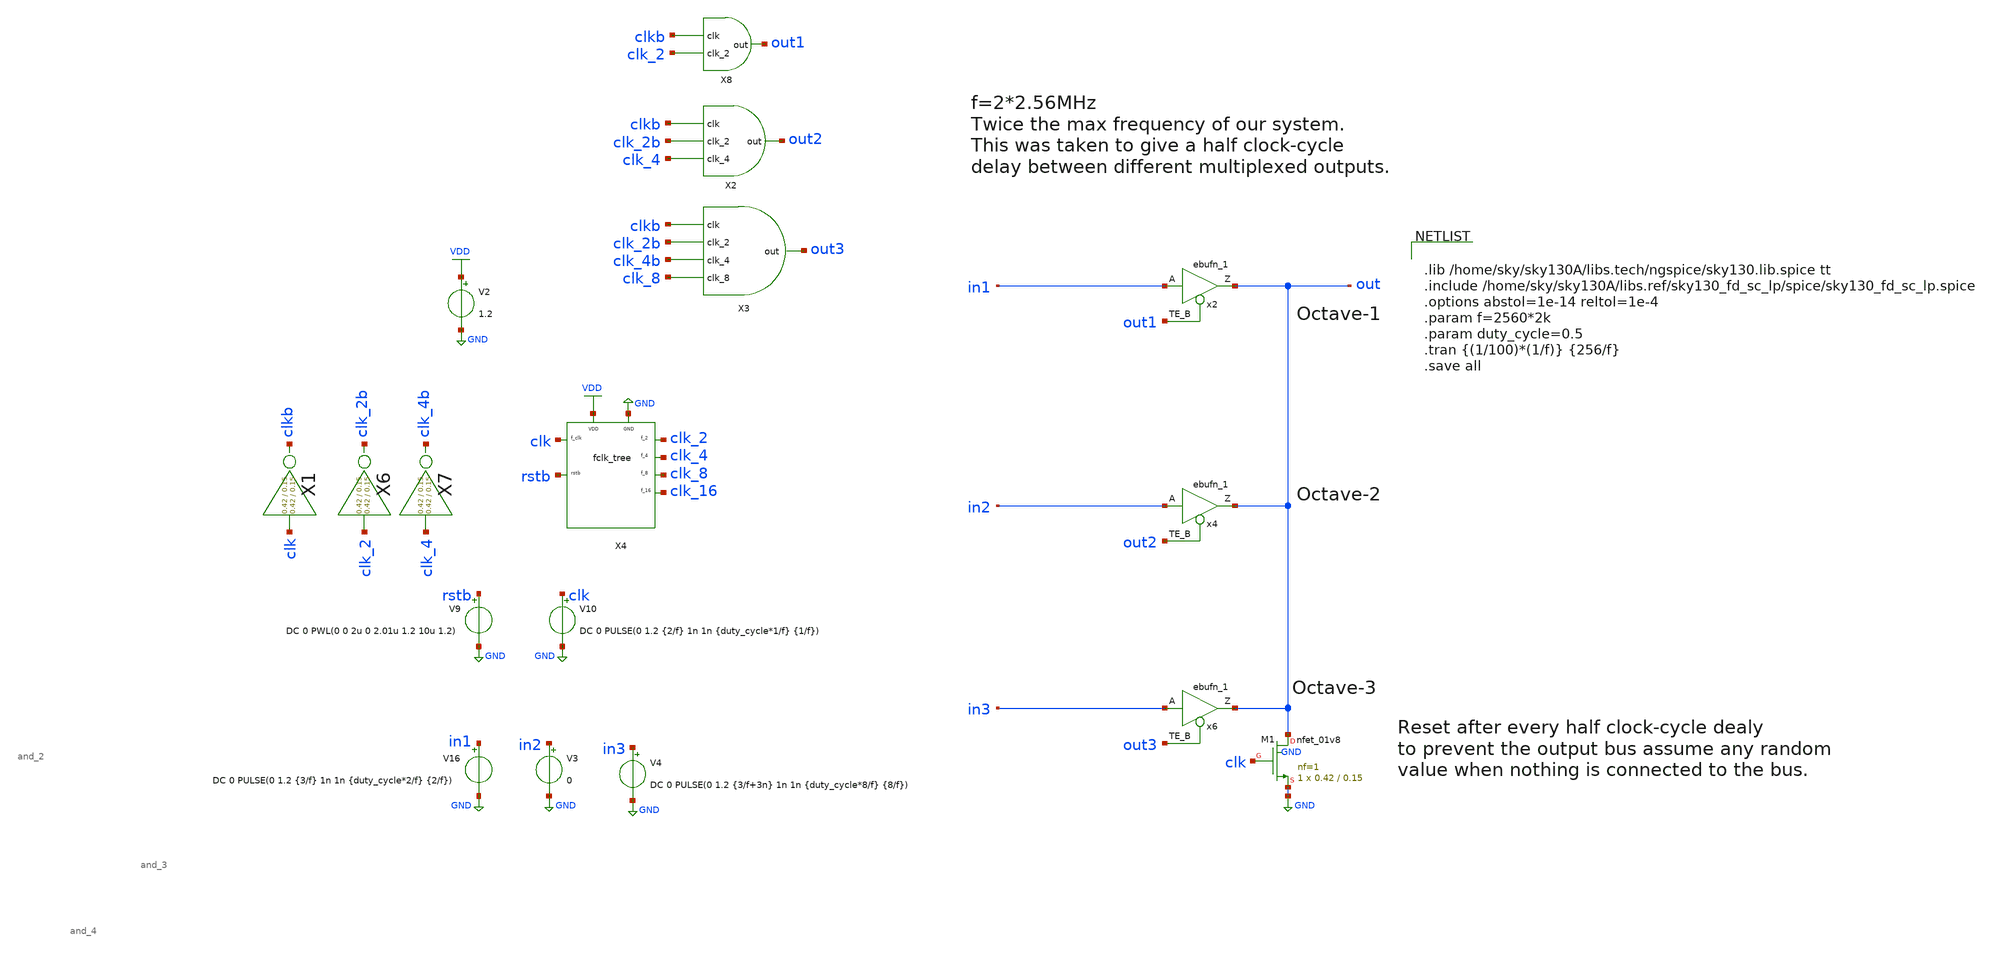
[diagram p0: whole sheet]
** sch_path: xschem/readout/sample_ro_2.sch
**.subckt sample_ro_2
V2 VDD GND 1.2
X4 clk rstb clk_2 clk_4 VDD GND clk_8 clk_16 fclk_tree
V10 clk GND DC 0 PULSE(0 1.2 {2/f} 1n 1n {duty_cycle*1/f} {1/f})
x4 in2 out2 GND GND VDD VDD out sky130_fd_sc_lp__ebufn_1
x6 in3 out3 GND GND VDD VDD out sky130_fd_sc_lp__ebufn_1
V9 rstb GND DC 0 PWL(0 0 2u 0 2.01u 1.2 10u 1.2)
x2 in1 out1 GND GND VDD VDD out sky130_fd_sc_lp__ebufn_1
XM1 out clk GND GND sky130_fd_pr__nfet_01v8 L=0.15 W=0.42 nf=1 ad='int((nf+1)/2) * W/nf * 0.29' as='int((nf+2)/2) * W/nf * 0.29'
+ pd='2*int((nf+1)/2) * (W/nf + 0.29)' ps='2*int((nf+2)/2) * (W/nf + 0.29)' nrd='0.29 / W' nrs='0.29 / W'
+ sa=0 sb=0 sd=0 mult=1 m=1
X1 clk clkb inv Wpmos=0.42 Lpmos=0.15 Wnmos=0.42 Lnmos=0.15
V16 in1 GND DC 0 PULSE(0 1.2 {3/f} 1n 1n {duty_cycle*2/f} {2/f})
V3 in2 GND 0
V4 in3 GND DC 0 PULSE(0 1.2 {3/f+3n} 1n 1n {duty_cycle*8/f} {8/f})
X6 clk_2 clk_2b inv Wpmos=0.42 Lpmos=0.15 Wnmos=0.42 Lnmos=0.15
X7 clk_4 clk_4b inv Wpmos=0.42 Lpmos=0.15 Wnmos=0.42 Lnmos=0.15
X8 clkb clk_2 out1 and_2
X2 clkb clk_2b clk_4 out2 and_3
X3 clkb clk_2b clk_4b clk_8 out3 and_4
**** begin user architecture code


.lib /home/sky/sky130A/libs.tech/ngspice/sky130.lib.spice tt
.include /home/sky/sky130A/libs.ref/sky130_fd_sc_lp/spice/sky130_fd_sc_lp.spice
.options abstol=1e-14 reltol=1e-4
.param f=2560*2k
.param duty_cycle=0.5
.tran {(1/100)*(1/f)} {256/f}
.save all


**** end user architecture code
**.ends

* expanding   symbol:  readout/fclk_tree.sym # of pins=8
** sym_path: xschem/readout/fclk_tree.sym
** sch_path: xschem/readout/fclk_tree.sch
.subckt fclk_tree f_clk rstb f_2 f_4 VDD GND f_8 f_16
*.iopin VDD
*.iopin GND
*.ipin rstb
*.opin f_2
*.opin f_4
*.opin f_8
*.opin f_16
*.ipin f_clk
x2 f_clk net1 rstb gnd gnd vdd vdd f_2 net1 sky130_fd_sc_lp__dfrbp_1
x4 f_2 net2 rstb gnd gnd vdd vdd f_4 net2 sky130_fd_sc_lp__dfrbp_1
x1 f_4 net3 rstb gnd gnd vdd vdd f_8 net3 sky130_fd_sc_lp__dfrbp_1
x6 f_8 net4 rstb gnd gnd vdd vdd f_16 net4 sky130_fd_sc_lp__dfrbp_1
.ends


* expanding   symbol:  inv/inv.sym # of pins=2
** sym_path: xschem/inv/inv.sym
** sch_path: xschem/inv/inv.sch
.subckt inv in out  Wpmos=3 Lpmos=0.18 Wnmos=1 Lnmos=0.18
*.ipin in
*.iopin out
XM1 out in GND GND sky130_fd_pr__nfet_01v8 L=Lnmos W=Wnmos nf=1 ad='int((nf+1)/2) * W/nf * 0.29' as='int((nf+2)/2) * W/nf * 0.29'
+ pd='2*int((nf+1)/2) * (W/nf + 0.29)' ps='2*int((nf+2)/2) * (W/nf + 0.29)' nrd='0.29 / W' nrs='0.29 / W'
+ sa=0 sb=0 sd=0 mult=1 m=1
XM2 out in VDD VDD sky130_fd_pr__pfet_01v8 L=Lpmos W=Wpmos nf=1 ad='int((nf+1)/2) * W/nf * 0.29' as='int((nf+2)/2) * W/nf * 0.29'
+ pd='2*int((nf+1)/2) * (W/nf + 0.29)' ps='2*int((nf+2)/2) * (W/nf + 0.29)' nrd='0.29 / W' nrs='0.29 / W'
+ sa=0 sb=0 sd=0 mult=1 m=1
.ends


* expanding   symbol:  and_set/and_2.sym # of pins=3
** sym_path: xschem/and_set/and_2.sym
** sch_path: xschem/and_set/and_2.sch
.subckt and_2 clk clk_2 out
*.ipin clk
*.ipin clk_2
*.opin out
XM1 out clk_2 VDD VDD sky130_fd_pr__pfet_01v8 L=0.15 W=0.42 nf=1 ad='int((nf+1)/2) * W/nf * 0.29' as='int((nf+2)/2) * W/nf * 0.29'
+ pd='2*int((nf+1)/2) * (W/nf + 0.29)' ps='2*int((nf+2)/2) * (W/nf + 0.29)' nrd='0.29 / W' nrs='0.29 / W'
+ sa=0 sb=0 sd=0 mult=1 m=1
XM2 out clk net1 GND sky130_fd_pr__nfet_01v8 L=0.15 W=0.42 nf=1 ad='int((nf+1)/2) * W/nf * 0.29' as='int((nf+2)/2) * W/nf * 0.29'
+ pd='2*int((nf+1)/2) * (W/nf + 0.29)' ps='2*int((nf+2)/2) * (W/nf + 0.29)' nrd='0.29 / W' nrs='0.29 / W'
+ sa=0 sb=0 sd=0 mult=1 m=1
XM3 net1 clk_2 GND GND sky130_fd_pr__nfet_01v8 L=0.15 W=0.42 nf=1 ad='int((nf+1)/2) * W/nf * 0.29' as='int((nf+2)/2) * W/nf * 0.29'
+ pd='2*int((nf+1)/2) * (W/nf + 0.29)' ps='2*int((nf+2)/2) * (W/nf + 0.29)' nrd='0.29 / W' nrs='0.29 / W'
+ sa=0 sb=0 sd=0 mult=1 m=1
XM14 out clk VDD VDD sky130_fd_pr__pfet_01v8 L=0.15 W=0.42 nf=1 ad='int((nf+1)/2) * W/nf * 0.29' as='int((nf+2)/2) * W/nf * 0.29'
+ pd='2*int((nf+1)/2) * (W/nf + 0.29)' ps='2*int((nf+2)/2) * (W/nf + 0.29)' nrd='0.29 / W' nrs='0.29 / W'
+ sa=0 sb=0 sd=0 mult=1 m=1
.ends


* expanding   symbol:  and_set/and_3.sym # of pins=4
** sym_path: xschem/and_set/and_3.sym
** sch_path: xschem/and_set/and_3.sch
.subckt and_3 clk clk_2 clk_4 out
*.ipin clk_2
*.ipin clk
*.ipin clk_4
*.opin out
XM1 out clk_2 VDD VDD sky130_fd_pr__pfet_01v8 L=0.15 W=0.42 nf=1 ad='int((nf+1)/2) * W/nf * 0.29' as='int((nf+2)/2) * W/nf * 0.29'
+ pd='2*int((nf+1)/2) * (W/nf + 0.29)' ps='2*int((nf+2)/2) * (W/nf + 0.29)' nrd='0.29 / W' nrs='0.29 / W'
+ sa=0 sb=0 sd=0 mult=1 m=1
XM2 out clk net1 GND sky130_fd_pr__nfet_01v8 L=0.15 W=0.42 nf=1 ad='int((nf+1)/2) * W/nf * 0.29' as='int((nf+2)/2) * W/nf * 0.29'
+ pd='2*int((nf+1)/2) * (W/nf + 0.29)' ps='2*int((nf+2)/2) * (W/nf + 0.29)' nrd='0.29 / W' nrs='0.29 / W'
+ sa=0 sb=0 sd=0 mult=1 m=1
XM3 net1 clk_2 net2 GND sky130_fd_pr__nfet_01v8 L=0.15 W=0.42 nf=1 ad='int((nf+1)/2) * W/nf * 0.29' as='int((nf+2)/2) * W/nf * 0.29'
+ pd='2*int((nf+1)/2) * (W/nf + 0.29)' ps='2*int((nf+2)/2) * (W/nf + 0.29)' nrd='0.29 / W' nrs='0.29 / W'
+ sa=0 sb=0 sd=0 mult=1 m=1
XM4 net2 clk_4 GND GND sky130_fd_pr__nfet_01v8 L=0.15 W=0.42 nf=1 ad='int((nf+1)/2) * W/nf * 0.29' as='int((nf+2)/2) * W/nf * 0.29'
+ pd='2*int((nf+1)/2) * (W/nf + 0.29)' ps='2*int((nf+2)/2) * (W/nf + 0.29)' nrd='0.29 / W' nrs='0.29 / W'
+ sa=0 sb=0 sd=0 mult=1 m=1
XM11 out clk_4 VDD VDD sky130_fd_pr__pfet_01v8 L=0.15 W=0.42 nf=1 ad='int((nf+1)/2) * W/nf * 0.29' as='int((nf+2)/2) * W/nf * 0.29'
+ pd='2*int((nf+1)/2) * (W/nf + 0.29)' ps='2*int((nf+2)/2) * (W/nf + 0.29)' nrd='0.29 / W' nrs='0.29 / W'
+ sa=0 sb=0 sd=0 mult=1 m=1
XM14 out clk VDD VDD sky130_fd_pr__pfet_01v8 L=0.15 W=0.42 nf=1 ad='int((nf+1)/2) * W/nf * 0.29' as='int((nf+2)/2) * W/nf * 0.29'
+ pd='2*int((nf+1)/2) * (W/nf + 0.29)' ps='2*int((nf+2)/2) * (W/nf + 0.29)' nrd='0.29 / W' nrs='0.29 / W'
+ sa=0 sb=0 sd=0 mult=1 m=1
.ends


* expanding   symbol:  and_set/and_4.sym # of pins=5
** sym_path: xschem/and_set/and_4.sym
** sch_path: xschem/and_set/and_4.sch
.subckt and_4 clk clk_2 clk_4 clk_8 out
*.ipin clk_2
*.ipin clk
*.ipin clk_4
*.ipin clk_8
*.opin out
XM1 out clk_2 VDD VDD sky130_fd_pr__pfet_01v8 L=0.15 W=0.42 nf=1 ad='int((nf+1)/2) * W/nf * 0.29' as='int((nf+2)/2) * W/nf * 0.29'
+ pd='2*int((nf+1)/2) * (W/nf + 0.29)' ps='2*int((nf+2)/2) * (W/nf + 0.29)' nrd='0.29 / W' nrs='0.29 / W'
+ sa=0 sb=0 sd=0 mult=1 m=1
XM2 out clk net1 GND sky130_fd_pr__nfet_01v8 L=0.15 W=0.42 nf=1 ad='int((nf+1)/2) * W/nf * 0.29' as='int((nf+2)/2) * W/nf * 0.29'
+ pd='2*int((nf+1)/2) * (W/nf + 0.29)' ps='2*int((nf+2)/2) * (W/nf + 0.29)' nrd='0.29 / W' nrs='0.29 / W'
+ sa=0 sb=0 sd=0 mult=1 m=1
XM3 net1 clk_2 net2 GND sky130_fd_pr__nfet_01v8 L=0.15 W=0.42 nf=1 ad='int((nf+1)/2) * W/nf * 0.29' as='int((nf+2)/2) * W/nf * 0.29'
+ pd='2*int((nf+1)/2) * (W/nf + 0.29)' ps='2*int((nf+2)/2) * (W/nf + 0.29)' nrd='0.29 / W' nrs='0.29 / W'
+ sa=0 sb=0 sd=0 mult=1 m=1
XM4 net2 clk_4 net3 GND sky130_fd_pr__nfet_01v8 L=0.15 W=0.42 nf=1 ad='int((nf+1)/2) * W/nf * 0.29' as='int((nf+2)/2) * W/nf * 0.29'
+ pd='2*int((nf+1)/2) * (W/nf + 0.29)' ps='2*int((nf+2)/2) * (W/nf + 0.29)' nrd='0.29 / W' nrs='0.29 / W'
+ sa=0 sb=0 sd=0 mult=1 m=1
XM5 net3 clk_8 GND GND sky130_fd_pr__nfet_01v8 L=0.15 W=0.42 nf=1 ad='int((nf+1)/2) * W/nf * 0.29' as='int((nf+2)/2) * W/nf * 0.29'
+ pd='2*int((nf+1)/2) * (W/nf + 0.29)' ps='2*int((nf+2)/2) * (W/nf + 0.29)' nrd='0.29 / W' nrs='0.29 / W'
+ sa=0 sb=0 sd=0 mult=1 m=1
XM11 out clk_4 VDD VDD sky130_fd_pr__pfet_01v8 L=0.15 W=0.42 nf=1 ad='int((nf+1)/2) * W/nf * 0.29' as='int((nf+2)/2) * W/nf * 0.29'
+ pd='2*int((nf+1)/2) * (W/nf + 0.29)' ps='2*int((nf+2)/2) * (W/nf + 0.29)' nrd='0.29 / W' nrs='0.29 / W'
+ sa=0 sb=0 sd=0 mult=1 m=1
XM12 out clk_8 VDD VDD sky130_fd_pr__pfet_01v8 L=0.15 W=0.42 nf=1 ad='int((nf+1)/2) * W/nf * 0.29' as='int((nf+2)/2) * W/nf * 0.29'
+ pd='2*int((nf+1)/2) * (W/nf + 0.29)' ps='2*int((nf+2)/2) * (W/nf + 0.29)' nrd='0.29 / W' nrs='0.29 / W'
+ sa=0 sb=0 sd=0 mult=1 m=1
XM14 out clk VDD VDD sky130_fd_pr__pfet_01v8 L=0.15 W=0.42 nf=1 ad='int((nf+1)/2) * W/nf * 0.29' as='int((nf+2)/2) * W/nf * 0.29'
+ pd='2*int((nf+1)/2) * (W/nf + 0.29)' ps='2*int((nf+2)/2) * (W/nf + 0.29)' nrd='0.29 / W' nrs='0.29 / W'
+ sa=0 sb=0 sd=0 mult=1 m=1
.ends

.GLOBAL GND
.GLOBAL VDD
.end
